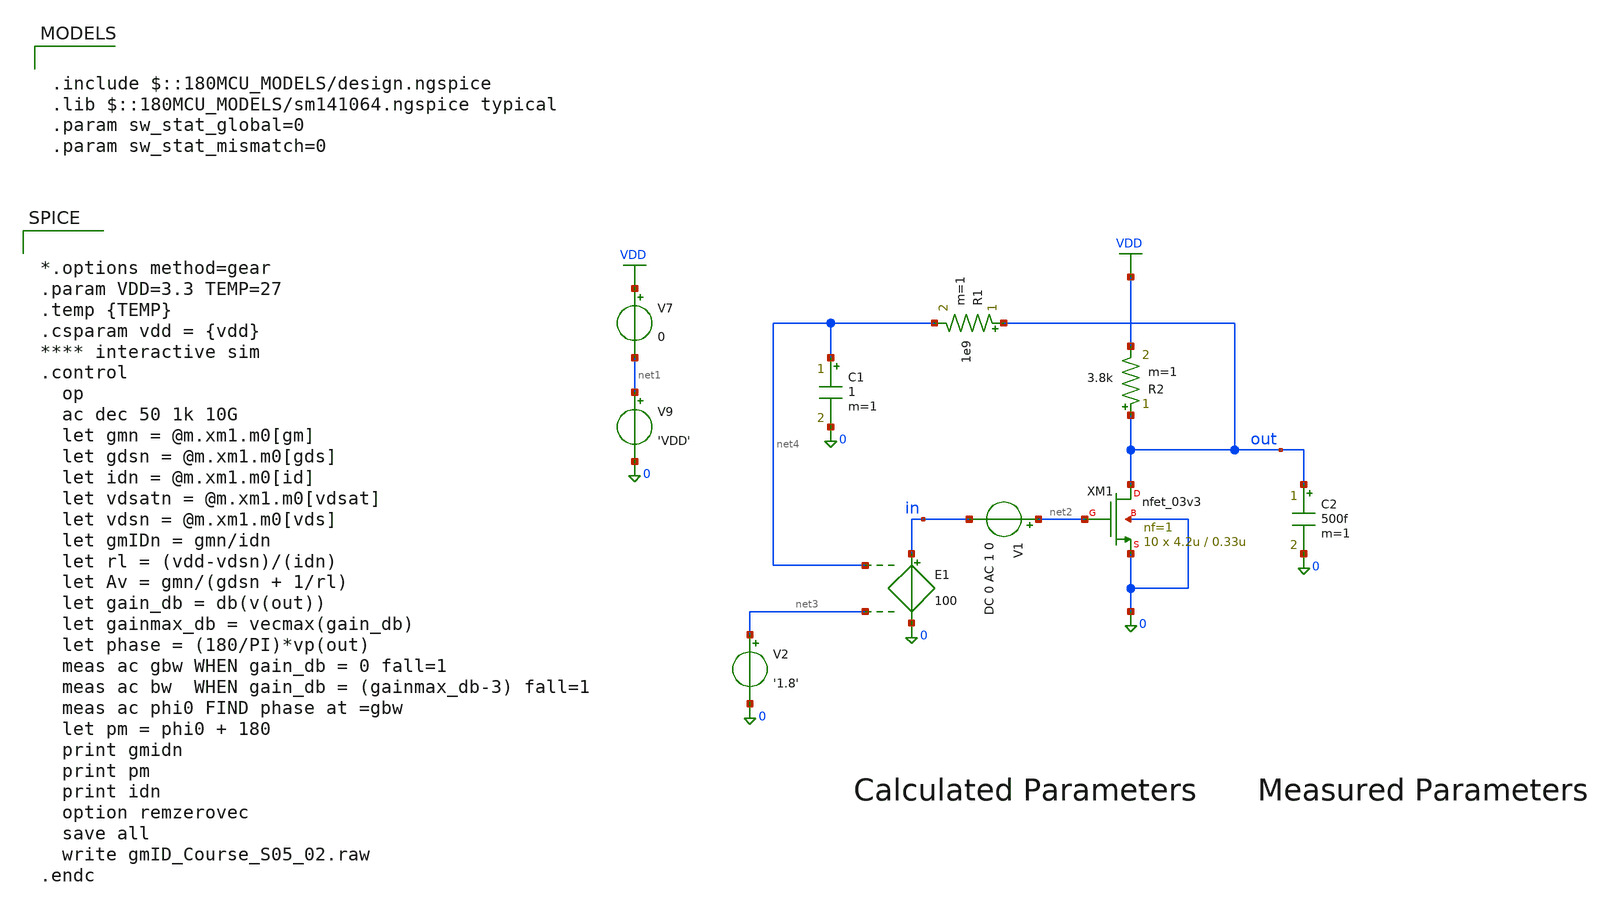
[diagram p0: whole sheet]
** sch_path: Xschem/gf180mcuD/gmID_Designs/gmID_Course_S05_02.sch
**.subckt gmID_Course_S05_02
XM1 out net2 0 0 nfet_03v3 L=0.33u W=4.2u nf=1 ad='int((nf+1)/2) * W/nf * 0.18u' as='int((nf+2)/2) * W/nf * 0.18u'
+ pd='2*int((nf+1)/2) * (W/nf + 0.18u)' ps='2*int((nf+2)/2) * (W/nf + 0.18u)' nrd='0.18u / W' nrs='0.18u / W'
+ sa=0 sb=0 sd=0 m=10
E1 in 0 net4 net3 100
R1 out net4 1e9 m=1
C1 net4 0 1 m=1
V1 net2 in DC 0 AC 1 0
V9 net1 0 'VDD'
V7 VDD net1 0
C2 out 0 500f m=1
V2 net3 0 '1.8'
R2 out VDD 3.8k m=1
**** begin user architecture code

.include $::180MCU_MODELS/design.ngspice
.lib $::180MCU_MODELS/sm141064.ngspice typical
.param sw_stat_global=0
.param sw_stat_mismatch=0



*.options method=gear
.param VDD=3.3 TEMP=27
.temp {TEMP}
.csparam vdd = {vdd}
**** interactive sim
.control
  op
  ac dec 50 1k 10G
  let gmn = @m.xm1.m0[gm]
  let gdsn = @m.xm1.m0[gds]
  let idn = @m.xm1.m0[id]
  let vdsatn = @m.xm1.m0[vdsat]
  let vdsn = @m.xm1.m0[vds]
  let gmIDn = gmn/idn
  let rl = (vdd-vdsn)/(idn)
  let Av = gmn/(gdsn + 1/rl)
  let gain_db = db(v(out))
  let gainmax_db = vecmax(gain_db)
  let phase = (180/PI)*vp(out)
  meas ac gbw WHEN gain_db = 0 fall=1
  meas ac bw  WHEN gain_db = (gainmax_db-3) fall=1
  meas ac phi0 FIND phase at =gbw
  let pm = phi0 + 180
  print gmidn
  print pm
  print idn
  option remzerovec
  save all
  write gmID_Course_S05_02.raw
.endc


**** end user architecture code
**.ends
.GLOBAL VDD
.end
